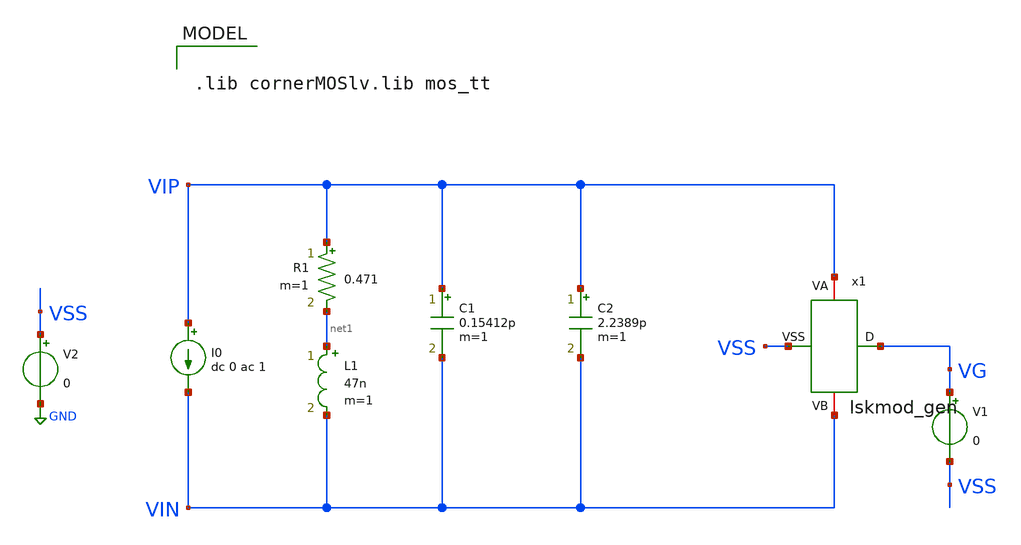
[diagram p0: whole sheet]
** sch_path: analog/tb/tb_lskmod_01.sch
**.subckt tb_lskmod_01
V2 VSS GND 0
V1 VG VSS 0
I0 VIP VIN dc 0 ac 1
C2 VIP VIN 2.2389p m=1
L1 net1 VIN 47n m=1
R1 VIP net1 0.471 m=1
C1 VIP VIN 0.15412p m=1
x1 VIP VSS VG VIN lskmod_gen
**** begin user architecture code


.lib cornerMOSlv.lib mos_tt





.save all
.save V(VIP) V(VIN) V(VIP, VIN)
.ac dec 1000 1Meg 1000Meg

.control
  set filetype=ascii        ; ASCII .raw (human-readable)
  run
  alter v1 dc = 1.2
  run
  let ZIN0  = ac1.v(VIP)-ac1.v(VIN)
  let ABSZ0 = abs(ZIN0)
  let IMZ0  = imag(ZIN0)
  let REZ0  = real(ZIN0)
  let Q0    = IMZ0/REZ0
  let ZIN1  = ac2.v(VIP)-ac2.v(VIN)
  let ABSZ1 = abs(ZIN1)
  let IMZ1  = imag(ZIN1)
  let REZ1  = real(ZIN1)
  let Q1    = IMZ1/REZ1
  write tb_lskmod_02.raw ABSZ0 Q0 ABSZ1 Q1
  set appendwrite
.endc


**** end user architecture code
**.ends

* expanding   symbol:  lskmod_gen.sym # of pins=4
** sym_path: analog/core/lskmod_gen.sym
** sch_path: analog/core/lskmod_gen.sch
.subckt lskmod_gen VA VSS D VB
*.iopin VA
*.iopin VSS
*.iopin D
*.iopin VB
XM1 VA D VB VSS sg13_lv_nmos w=1u l=0.13u ng=1 m=1 mm_ok=1
.ends

.GLOBAL GND
.end
